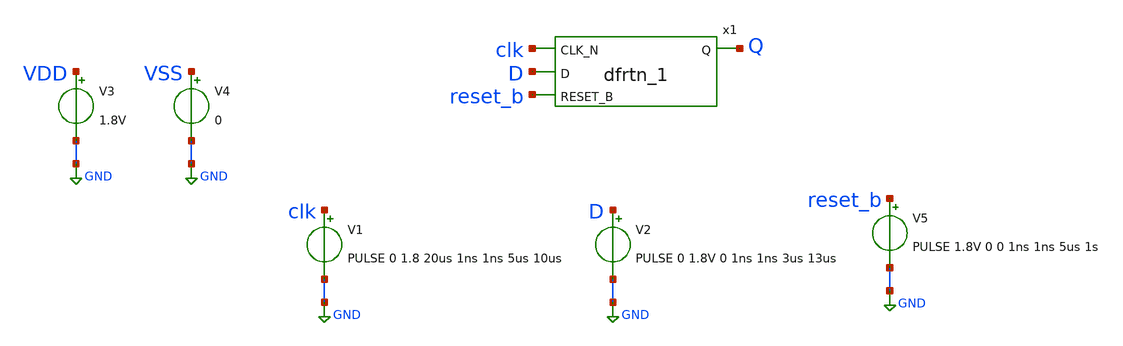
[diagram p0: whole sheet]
** sch_path: xschem/tests/dummy.sch
**.subckt dummy
V3 VDD GND 1.8V
V4 VSS GND 0
x1 clk D reset_b VSS VSS VDD VDD Q sky130_fd_sc_hd__dfrtn_1
V1 clk GND PULSE 0 1.8 20us 1ns 1ns 5us 10us
V2 D GND PULSE 0 1.8V 0 1ns 1ns 3us 13us
V5 reset_b GND PULSE 1.8V 0 0 1ns 1ns 5us 1s
**** begin user architecture code
 .lib $::SKYWATER_MODELS/sky130.lib.spice tt
.include $::SKYWATER_STDCELLS/sky130_fd_sc_hd.spice


.options acct list
.temp 25
*vvcc VDD 0 dc 1.8
*vvss VSS 0 0
.control
tran 0.1u 100u
*plot RST_PLS clk+2 Pulse+4
plot reset_b-2 clk D+2 Q+4
write dummy.raw
.endc


**** end user architecture code
**.ends
.GLOBAL GND
.end
